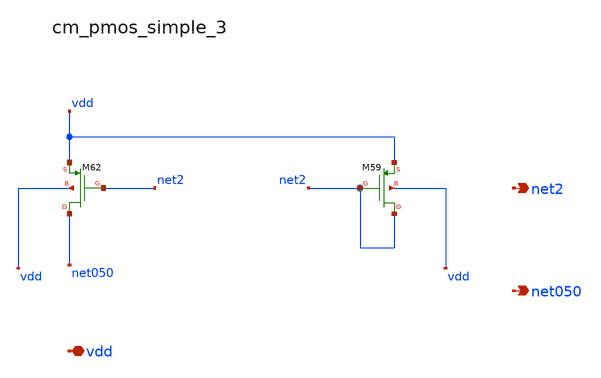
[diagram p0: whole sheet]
** sch_path: analog-db/raw/amp_005_hoilee_affc/hier/blocks/cm_pmos_simple_3.sch
**.subckt cm_pmos_simple_3 vdd net2 net050
*.iopin vdd
*.opin net2
*.opin net050
XM59 net2 net2 vdd vdd sg13_lv_pmos w=x_dut_xm59_w l=x_dut_xm59_l ng=1 m=x_dut_xm59_m
XM62 net050 net2 vdd vdd sg13_lv_pmos w=x_dut_xm62_w l=x_dut_xm62_l ng=1 m=x_dut_xm62_m
**.ends
.end
